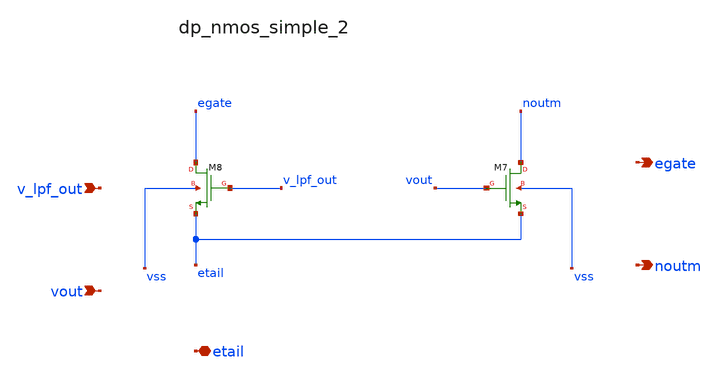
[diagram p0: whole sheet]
** sch_path: analog-db/raw/ldo_005_buffered_ref/hier/blocks/dp_nmos_simple_2.sch
**.subckt dp_nmos_simple_2 v_lpf_out vout etail egate noutm
*.ipin v_lpf_out
*.ipin vout
*.iopin etail
*.opin egate
*.opin noutm
XM7 noutm vout etail vss sg13_lv_nmos w=x_dut_xm7_w l=x_dut_xm7_l ng=1 m=1
XM8 egate v_lpf_out etail vss sg13_lv_nmos w=x_dut_xm8_w l=x_dut_xm8_l ng=1 m=1
**.ends
.end
